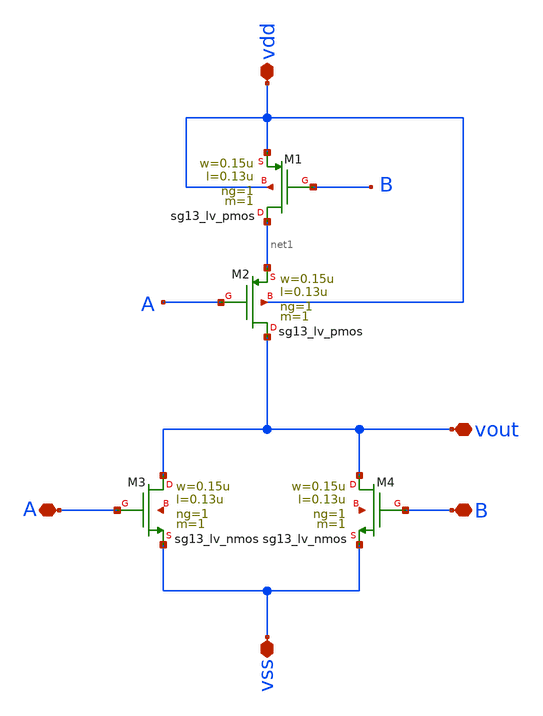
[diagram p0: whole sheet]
** sch_path: design/blocks/puertanor/puertanor.sch
**.subckt puertanor vdd vout B vss A
*.iopin vdd
*.iopin vout
*.iopin B
*.iopin vss
*.iopin A
XM1 net1 B vdd vdd sg13_lv_pmos w=0.15u l=0.13u ng=1 m=1 mm_ok=1
XM2 vout A net1 vdd sg13_lv_pmos w=0.15u l=0.13u ng=1 m=1 mm_ok=1
XM3 vout A vss net2 sg13_lv_nmos w=0.15u l=0.13u ng=1 m=1 mm_ok=1
XM4 vout B vss net3 sg13_lv_nmos w=0.15u l=0.13u ng=1 m=1 mm_ok=1
**.ends
.end
